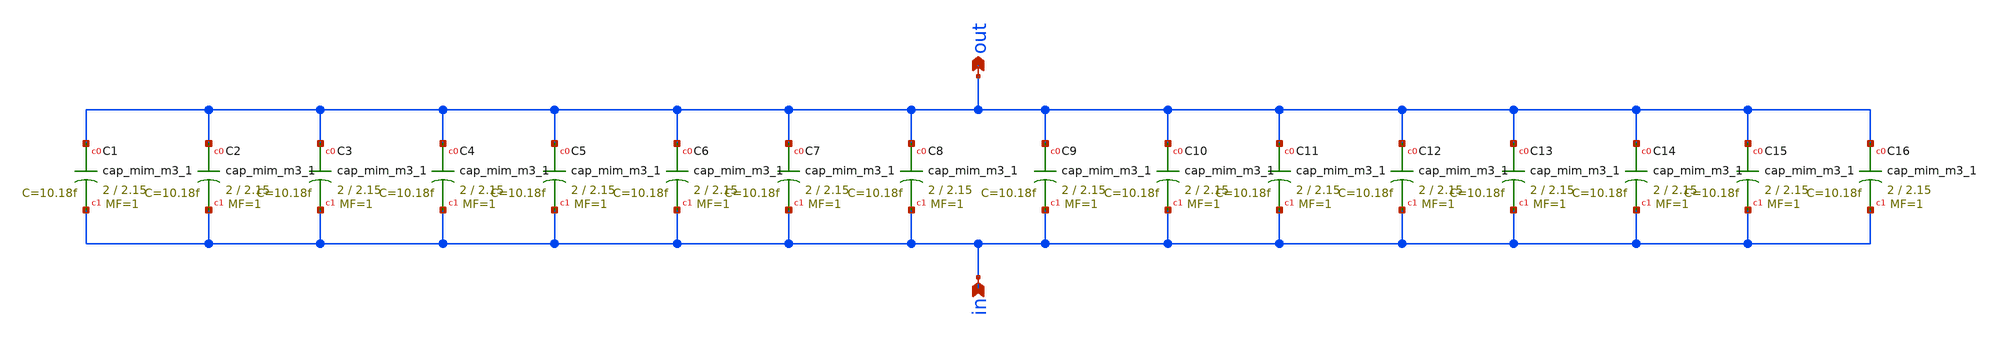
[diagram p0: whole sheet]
** sch_path: xschem/cap16.sch
**.subckt cap16 in out
*.ipin in
*.opin out
XC1 out in sky130_fd_pr__cap_mim_m3_1 W=2 L=2.15 MF=1 m=1
XC2 out in sky130_fd_pr__cap_mim_m3_1 W=2 L=2.15 MF=1 m=1
XC3 out in sky130_fd_pr__cap_mim_m3_1 W=2 L=2.15 MF=1 m=1
XC4 out in sky130_fd_pr__cap_mim_m3_1 W=2 L=2.15 MF=1 m=1
XC5 out in sky130_fd_pr__cap_mim_m3_1 W=2 L=2.15 MF=1 m=1
XC6 out in sky130_fd_pr__cap_mim_m3_1 W=2 L=2.15 MF=1 m=1
XC7 out in sky130_fd_pr__cap_mim_m3_1 W=2 L=2.15 MF=1 m=1
XC8 out in sky130_fd_pr__cap_mim_m3_1 W=2 L=2.15 MF=1 m=1
XC9 out in sky130_fd_pr__cap_mim_m3_1 W=2 L=2.15 MF=1 m=1
XC10 out in sky130_fd_pr__cap_mim_m3_1 W=2 L=2.15 MF=1 m=1
XC11 out in sky130_fd_pr__cap_mim_m3_1 W=2 L=2.15 MF=1 m=1
XC12 out in sky130_fd_pr__cap_mim_m3_1 W=2 L=2.15 MF=1 m=1
XC13 out in sky130_fd_pr__cap_mim_m3_1 W=2 L=2.15 MF=1 m=1
XC14 out in sky130_fd_pr__cap_mim_m3_1 W=2 L=2.15 MF=1 m=1
XC15 out in sky130_fd_pr__cap_mim_m3_1 W=2 L=2.15 MF=1 m=1
XC16 out in sky130_fd_pr__cap_mim_m3_1 W=2 L=2.15 MF=1 m=1
**.ends
.end
